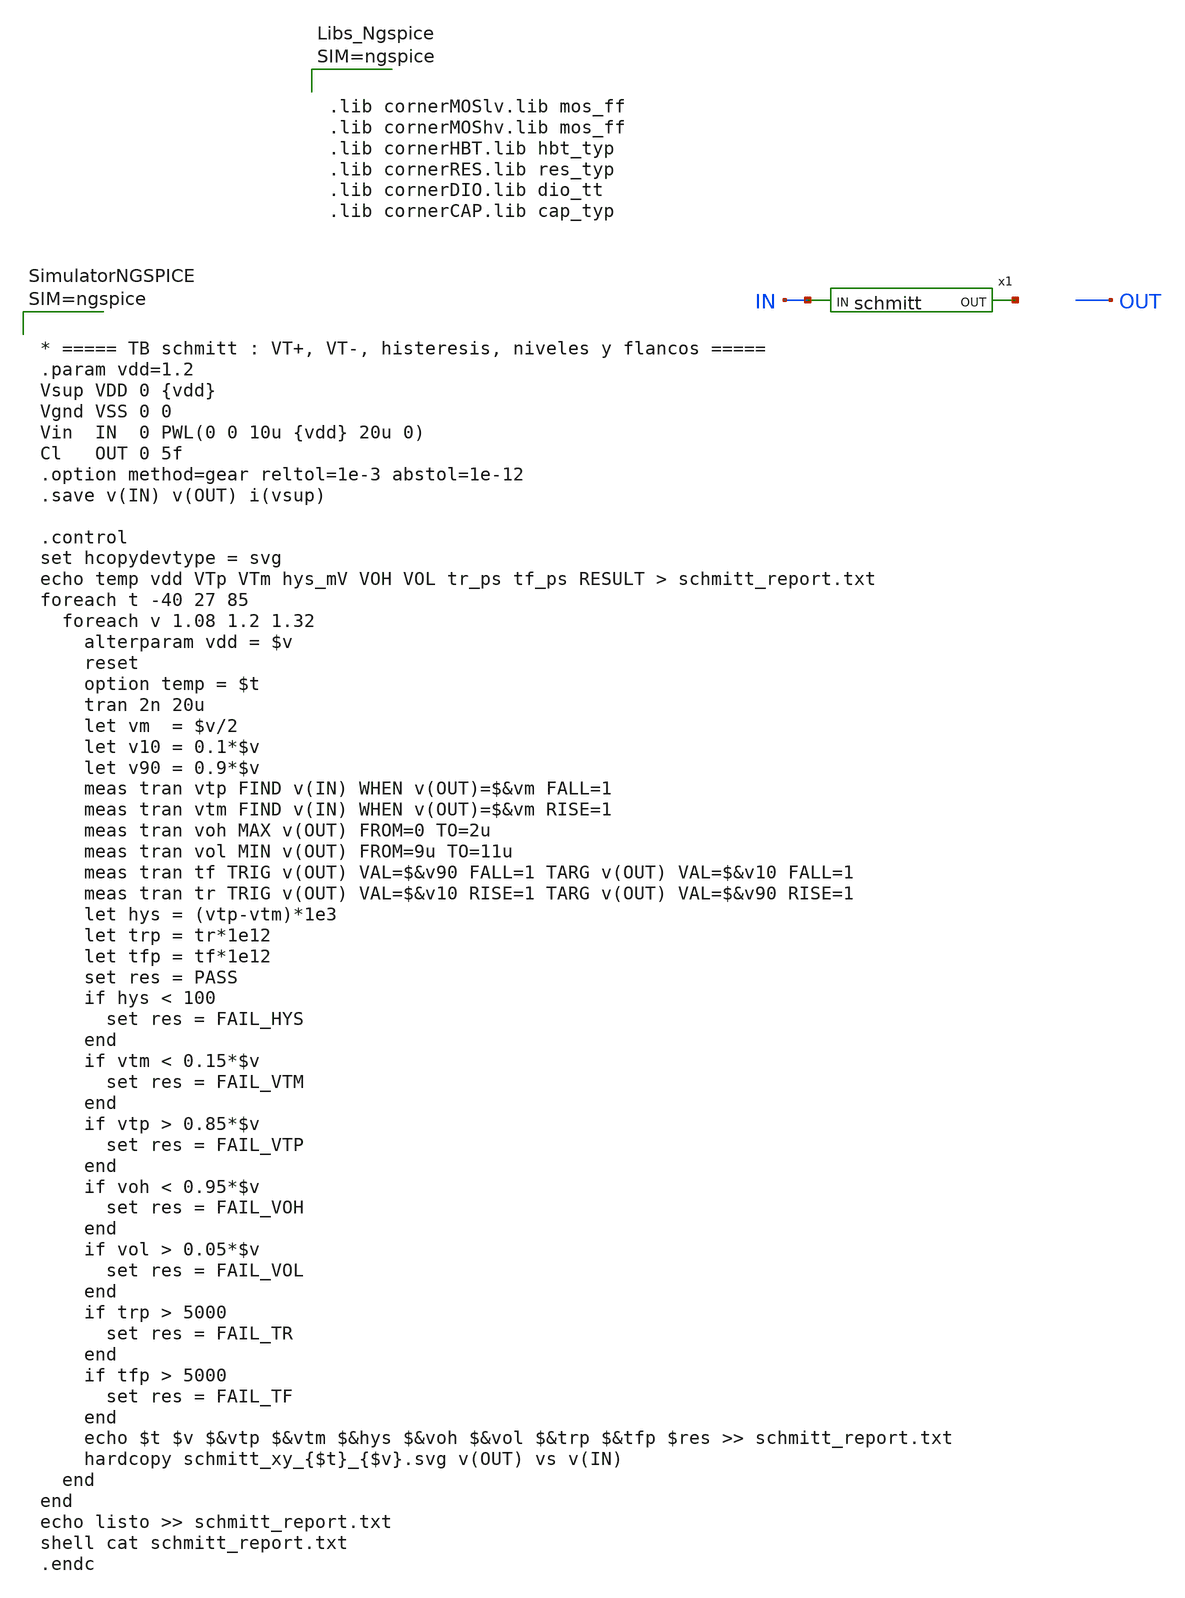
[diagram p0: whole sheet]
** sch_path: design/blocks/schmitt/schematic/schmitt_tb.sch
**.subckt schmitt_tb
x1 IN net1 VDD VSS schmitt
**** begin user architecture code



.lib cornerMOSlv.lib mos_ff
.lib cornerMOShv.lib mos_ff
.lib cornerHBT.lib hbt_typ
.lib cornerRES.lib res_typ
.lib cornerDIO.lib dio_tt
.lib cornerCAP.lib cap_typ






* ===== TB schmitt : VT+, VT-, histeresis, niveles y flancos =====
.param vdd=1.2
Vsup VDD 0 {vdd}
Vgnd VSS 0 0
Vin  IN  0 PWL(0 0 10u {vdd} 20u 0)
Cl   OUT 0 5f
.option method=gear reltol=1e-3 abstol=1e-12
.save v(IN) v(OUT) i(vsup)

.control
set hcopydevtype = svg
echo temp vdd VTp VTm hys_mV VOH VOL tr_ps tf_ps RESULT > schmitt_report.txt
foreach t -40 27 85
  foreach v 1.08 1.2 1.32
    alterparam vdd = $v
    reset
    option temp = $t
    tran 2n 20u
    let vm  = $v/2
    let v10 = 0.1*$v
    let v90 = 0.9*$v
    meas tran vtp FIND v(IN) WHEN v(OUT)=$&vm FALL=1
    meas tran vtm FIND v(IN) WHEN v(OUT)=$&vm RISE=1
    meas tran voh MAX v(OUT) FROM=0 TO=2u
    meas tran vol MIN v(OUT) FROM=9u TO=11u
    meas tran tf TRIG v(OUT) VAL=$&v90 FALL=1 TARG v(OUT) VAL=$&v10 FALL=1
    meas tran tr TRIG v(OUT) VAL=$&v10 RISE=1 TARG v(OUT) VAL=$&v90 RISE=1
    let hys = (vtp-vtm)*1e3
    let trp = tr*1e12
    let tfp = tf*1e12
    set res = PASS
    if hys < 100
      set res = FAIL_HYS
    end
    if vtm < 0.15*$v
      set res = FAIL_VTM
    end
    if vtp > 0.85*$v
      set res = FAIL_VTP
    end
    if voh < 0.95*$v
      set res = FAIL_VOH
    end
    if vol > 0.05*$v
      set res = FAIL_VOL
    end
    if trp > 5000
      set res = FAIL_TR
    end
    if tfp > 5000
      set res = FAIL_TF
    end
    echo $t $v $&vtp $&vtm $&hys $&voh $&vol $&trp $&tfp $res >> schmitt_report.txt
    hardcopy schmitt_xy_{$t}_{$v}.svg v(OUT) vs v(IN)
  end
end
echo listo >> schmitt_report.txt
shell cat schmitt_report.txt
.endc



**** end user architecture code
**.ends

* expanding   symbol:  schmitt.sym # of pins=2
** sym_path: design/blocks/schmitt/schematic/schmitt.sym
** sch_path: design/blocks/schmitt/schematic/schmitt.sch
.subckt schmitt IN OUT VDD VSS
*.opin OUT
*.ipin IN
XM4 net1 IN VDD VDD sg13_lv_pmos w=1.04u l=0.13u ng=1 m=1 mm_ok=1
XM6 OUT IN net2 VSS sg13_lv_nmos w=0.76u l=0.13u ng=1 m=1 mm_ok=1
XM5 OUT IN net1 VDD sg13_lv_pmos w=1.04u l=0.13u ng=1 m=1 mm_ok=1
XM7 net2 IN VSS VSS sg13_lv_nmos w=0.76u l=0.13u ng=1 m=1 mm_ok=1
XM8 VSS OUT net1 VDD sg13_lv_pmos w=0.42u l=0.13u ng=1 m=1 mm_ok=1
XM9 VDD OUT net2 VSS sg13_lv_nmos w=0.42u l=0.13u ng=1 m=1 mm_ok=1
.ends

.end
